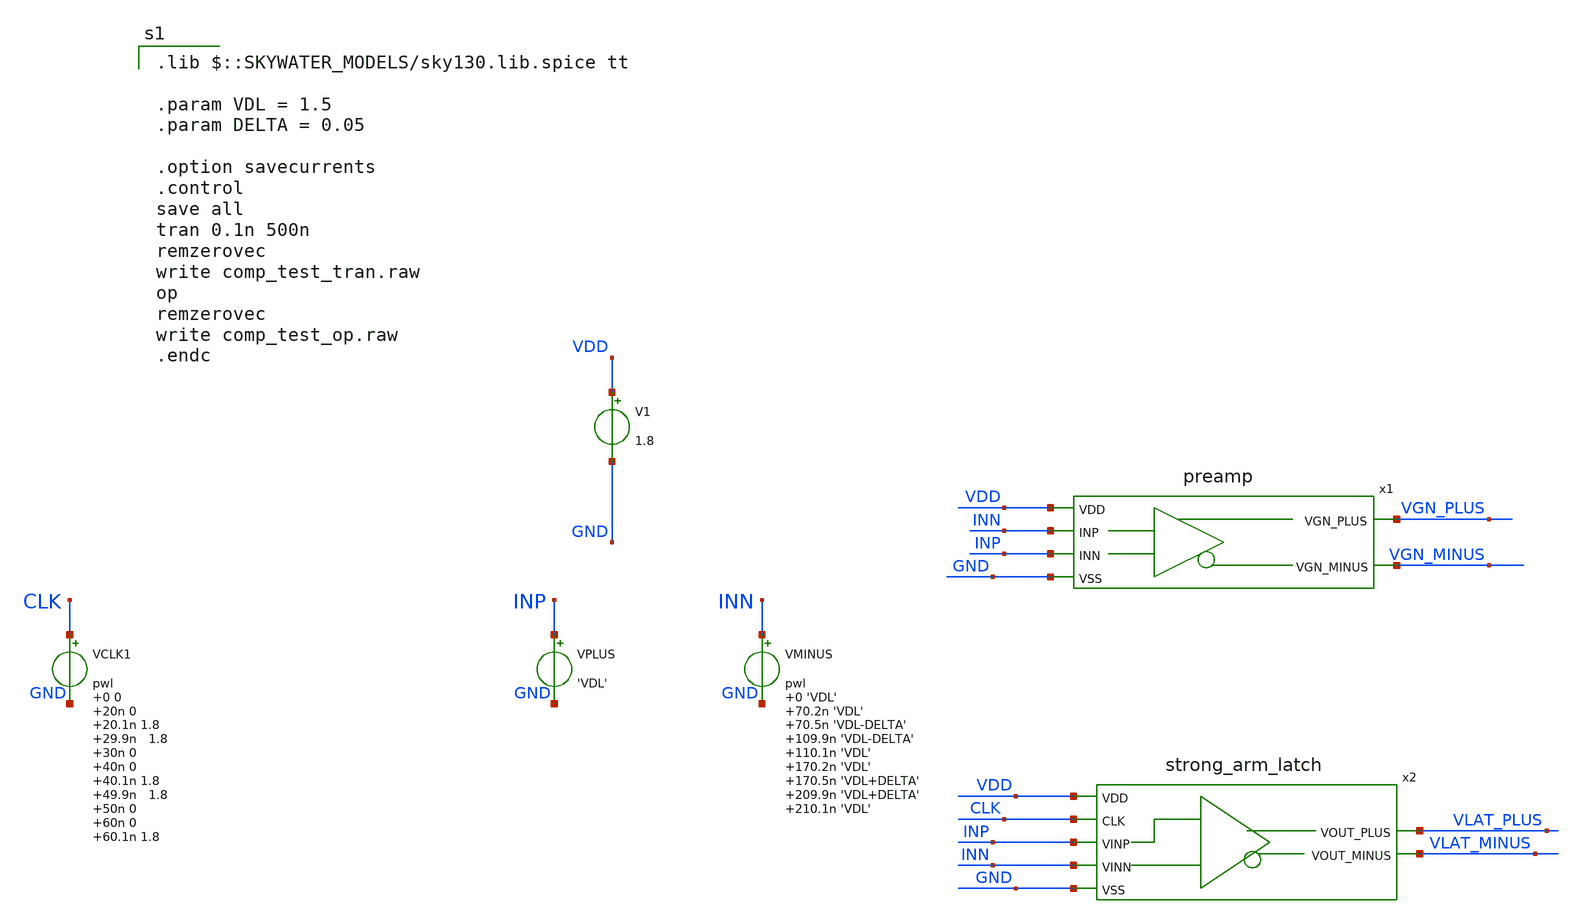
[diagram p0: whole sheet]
** sch_path: high_speed_comp_test.sch
**.subckt high_speed_comp_test
V1 VDD GND 1.8
VPLUS INP GND 'VDL'
VMINUS INN GND pwl 0 'VDL' 70.2n 'VDL' 70.5n 'VDL-DELTA' 109.9n 'VDL-DELTA' 110.1n 'VDL' 170.2n 'VDL'
+ 170.5n 'VDL+DELTA' 209.9n 'VDL+DELTA' 210.1n 'VDL'
x1 VDD VGN_PLUS VGN_MINUS INN INP GND preamp
x2 VDD CLK VLAT_PLUS VLAT_MINUS GND INP INN strong_arm_latch
VCLK1 CLK GND pwl 0 0 20n 0 20.1n 1.8 29.9n 1.8 30n 0 40n 0 40.1n 1.8 49.9n 1.8 50n 0 60n 0 60.1n
+ 1.8 69.9n 1.8 70n 0 80n 0 80.1n 1.8 89.9n 1.8 90n 0 100n 0 100.1n 1.8 109.9n 1.8 110n 0 120n 0 120.1n
+ 1.8 129.9n 1.8 130n 0 140n 0 140.1n 1.8 149.9n 1.8 150n 0 160n 0 160.1n 1.8 169.9n 1.8 170n 0 180n 0
+ 180.1n 1.8 189.9n 1.8 190n 0 200n 0 200.1n 1.8 209.9n 1.8 210n 0 220n 0 220.1n 1.8 229.9n 1.8 230n 0 240n
+ 0

**** begin user architecture code
 .lib $::SKYWATER_MODELS/sky130.lib.spice tt

.param VDL = 1.5
.param DELTA = 0.05

.option savecurrents
.control
save all
tran 0.1n 500n
remzerovec
write comp_test_tran.raw
op
remzerovec
write comp_test_op.raw
.endc



**** end user architecture code
**.ends
.end
